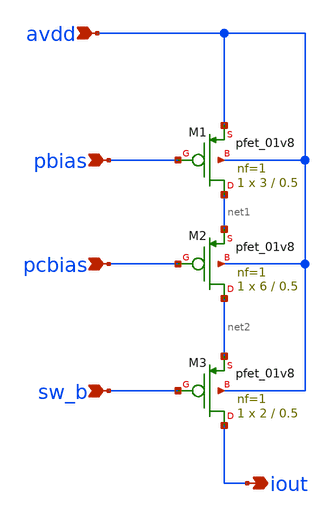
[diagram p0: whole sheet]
** sch_path: xsch/idac/pcell1s.sch
**.subckt pcell1s pbias pcbias avdd iout sw_b
*.ipin pbias
*.ipin pcbias
*.ipin avdd
*.opin iout
*.ipin sw_b
XM1 net1 pbias avdd avdd sky130_fd_pr__pfet_01v8 L=0.5 W=3 nf=1 ad='int((nf+1)/2) * W/nf * 0.29' as='int((nf+2)/2) * W/nf * 0.29'
+ pd='2*int((nf+1)/2) * (W/nf + 0.29)' ps='2*int((nf+2)/2) * (W/nf + 0.29)' nrd='0.29 / W' nrs='0.29 / W'
+ sa=0 sb=0 sd=0 mult=1 m=1
XM2 net2 pcbias net1 avdd sky130_fd_pr__pfet_01v8 L=0.5 W=6 nf=1 ad='int((nf+1)/2) * W/nf * 0.29' as='int((nf+2)/2) * W/nf * 0.29'
+ pd='2*int((nf+1)/2) * (W/nf + 0.29)' ps='2*int((nf+2)/2) * (W/nf + 0.29)' nrd='0.29 / W' nrs='0.29 / W'
+ sa=0 sb=0 sd=0 mult=1 m=1
XM3 iout sw_b net2 avdd sky130_fd_pr__pfet_01v8 L=0.5 W=2 nf=1 ad='int((nf+1)/2) * W/nf * 0.29' as='int((nf+2)/2) * W/nf * 0.29'
+ pd='2*int((nf+1)/2) * (W/nf + 0.29)' ps='2*int((nf+2)/2) * (W/nf + 0.29)' nrd='0.29 / W' nrs='0.29 / W'
+ sa=0 sb=0 sd=0 mult=1 m=1
**.ends
.end
